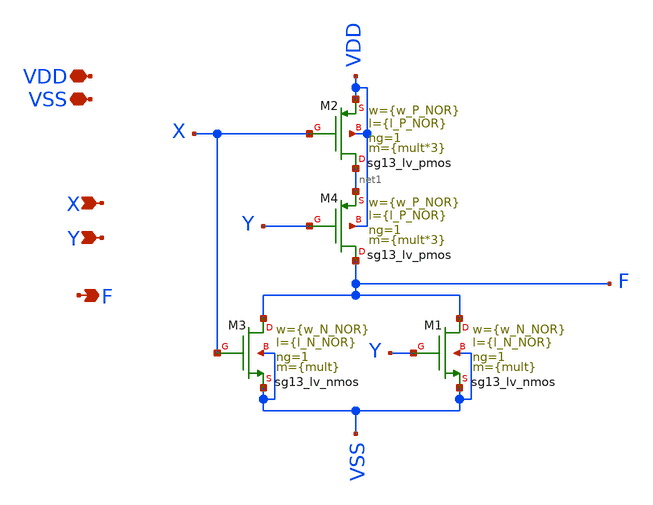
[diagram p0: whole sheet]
** sch_path: xschem/DigitalGates/NOR.sch
**.subckt NOR VDD X F VSS Y
*.iopin VDD
*.ipin X
*.opin F
*.iopin VSS
*.ipin Y
XM1 F Y VSS VSS sg13_lv_nmos w={w_N_NOR} l={l_N_NOR} ng=1 m={mult} mm_ok=1
XM2 net1 X VDD VDD sg13_lv_pmos w={w_P_NOR} l={l_P_NOR} ng=1 m={mult*3} mm_ok=1
XM4 F Y net1 VDD sg13_lv_pmos w={w_P_NOR} l={l_P_NOR} ng=1 m={mult*3} mm_ok=1
XM3 F X VSS VSS sg13_lv_nmos w={w_N_NOR} l={l_N_NOR} ng=1 m={mult} mm_ok=1
**** begin user architecture code



**** end user architecture code
**.ends
.end
